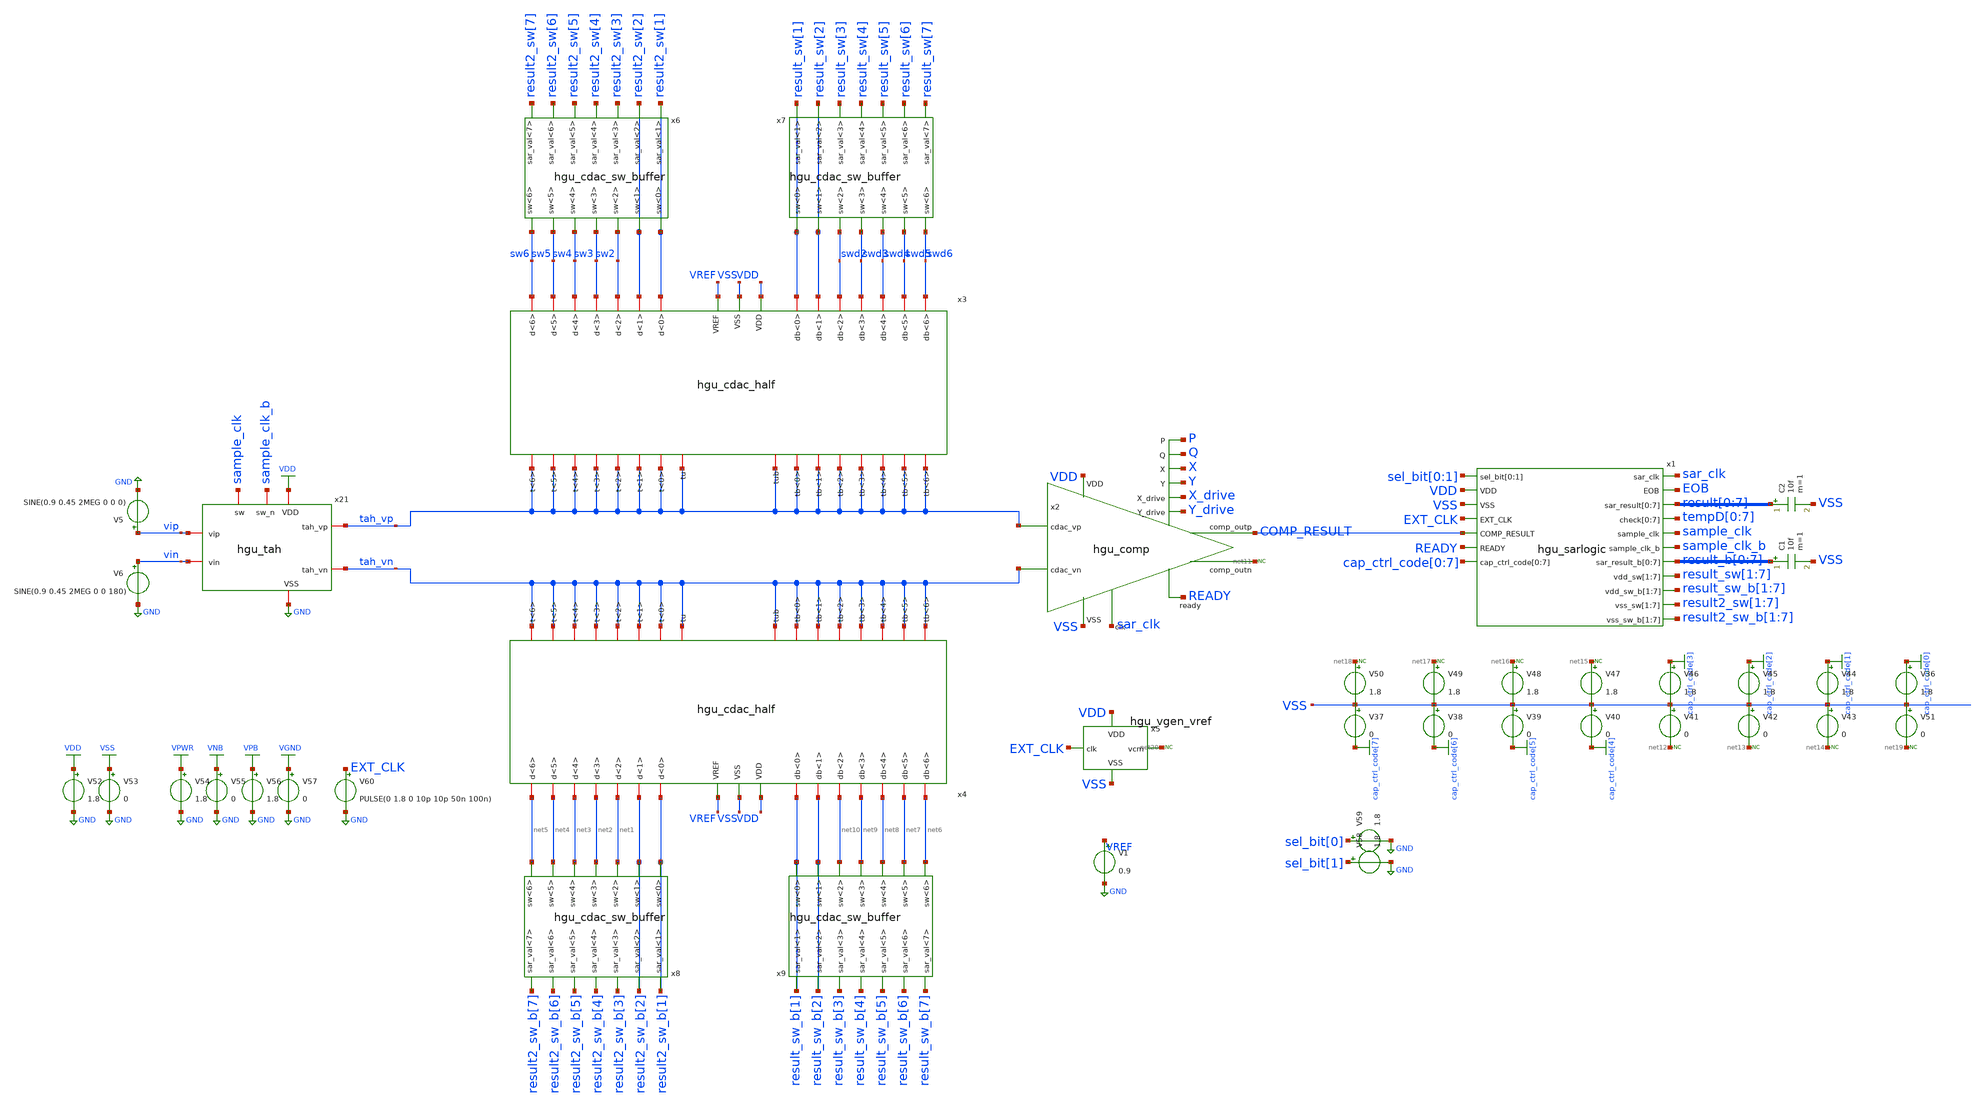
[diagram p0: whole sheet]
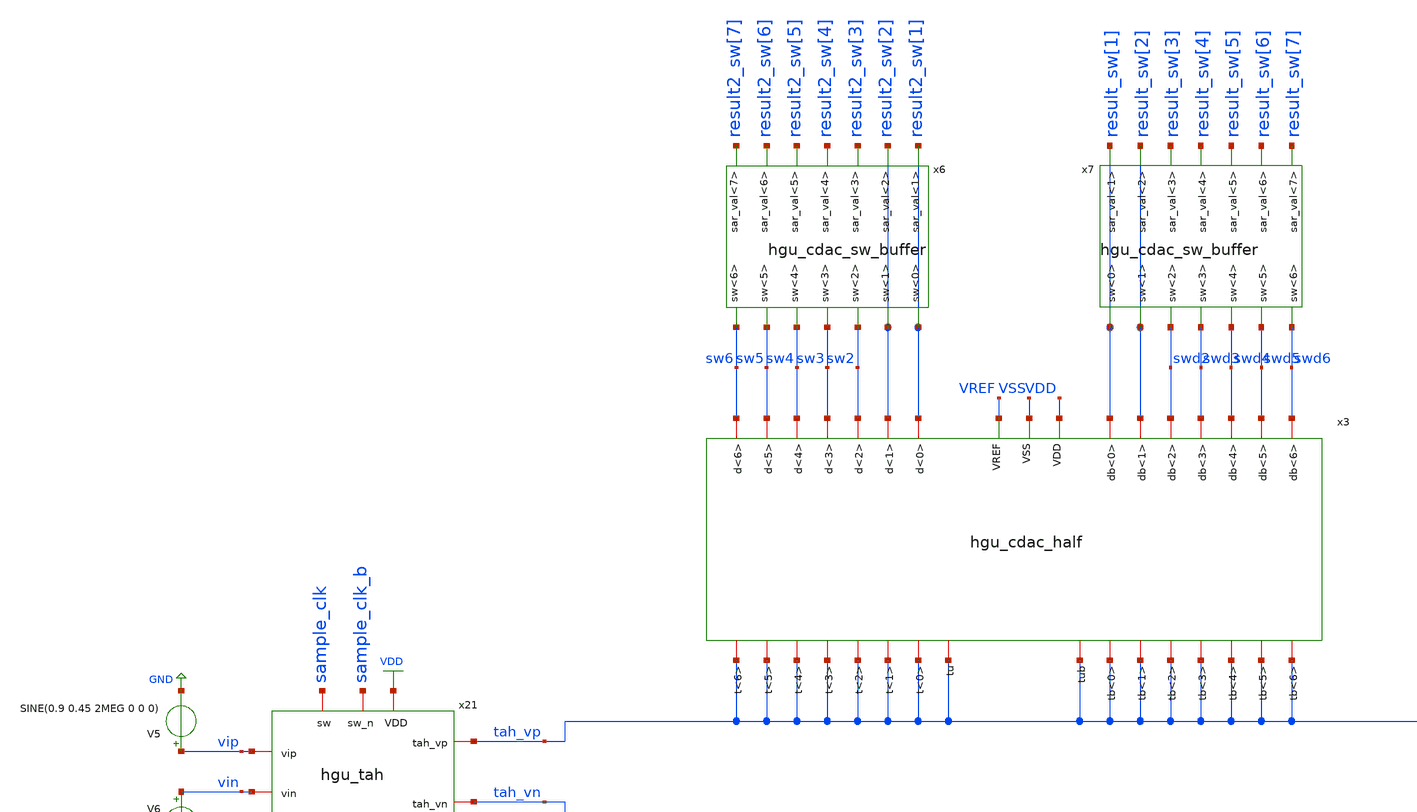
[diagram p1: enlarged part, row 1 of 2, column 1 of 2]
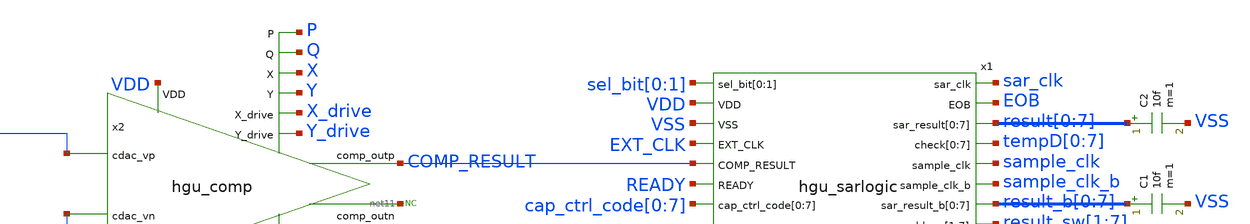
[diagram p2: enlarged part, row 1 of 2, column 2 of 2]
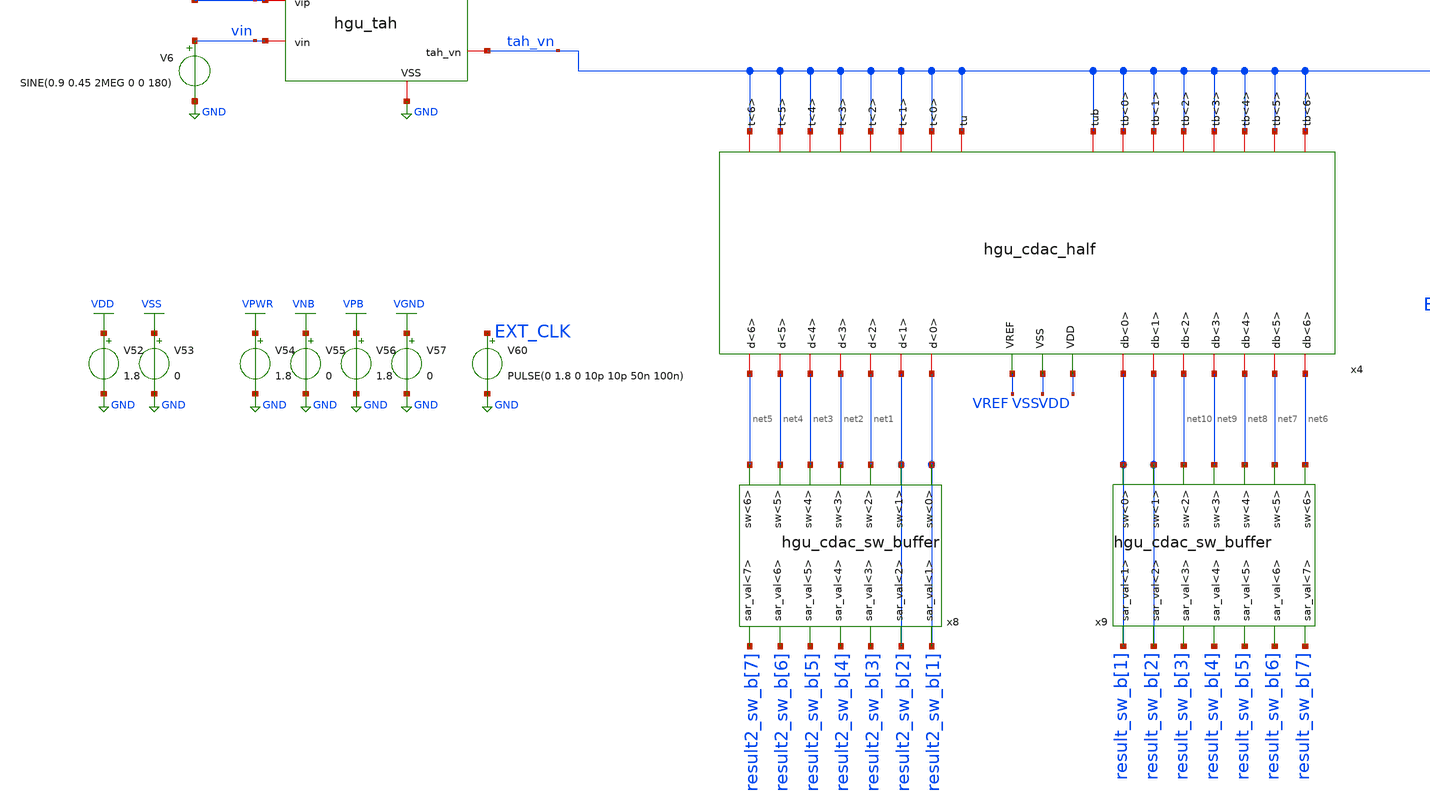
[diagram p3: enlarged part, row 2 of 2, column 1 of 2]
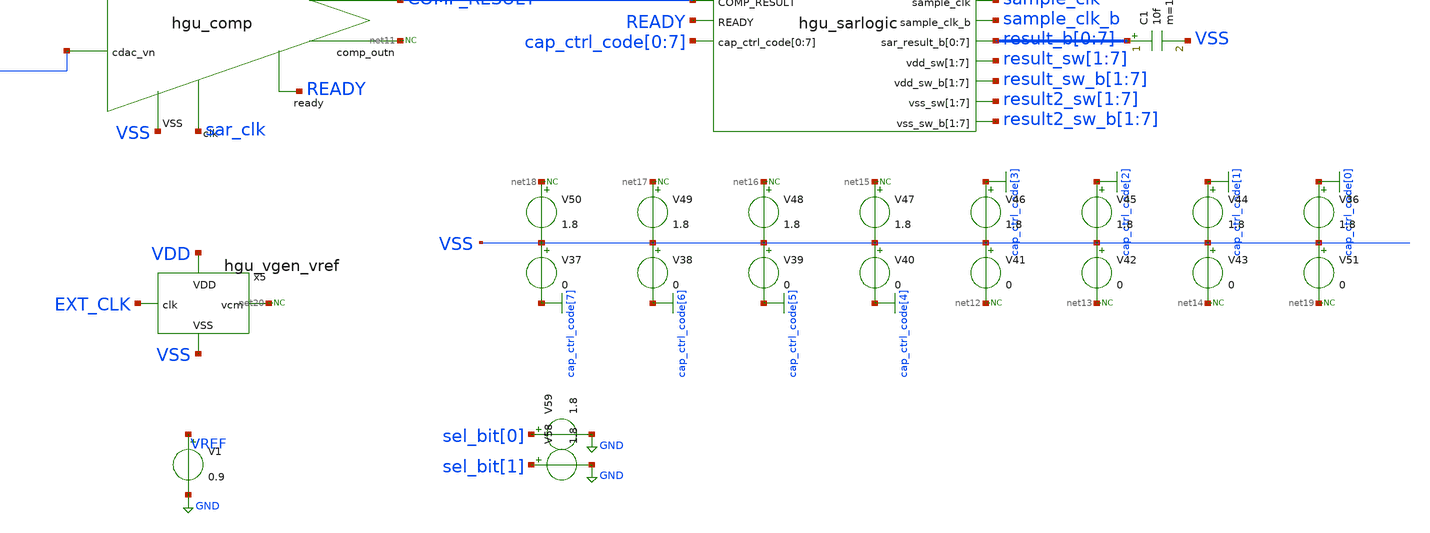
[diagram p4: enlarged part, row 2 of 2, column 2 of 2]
** sch_path: hgu/xschem/hgu_top.sch
**.subckt hgu_top
x1 sar_clk EOB result[0] result[1] result[2] result[3] result[4] result[5] result[6] result[7]
+ tempD[0] tempD[1] tempD[2] tempD[3] tempD[4] tempD[5] tempD[6] tempD[7] sample_clk sel_bit[0] sel_bit[1]
+ sample_clk_b VDD result_b[0] result_b[1] result_b[2] result_b[3] result_b[4] result_b[5] result_b[6] result_b[7]
+ VSS EXT_CLK COMP_RESULT READY result_sw[1] result_sw[2] result_sw[3] result_sw[4] result_sw[5]
+ result_sw[6] result_sw[7] result_sw_b[1] result_sw_b[2] result_sw_b[3] result_sw_b[4] result_sw_b[5]
+ result_sw_b[6] result_sw_b[7] result2_sw[1] result2_sw[2] result2_sw[3] result2_sw[4] result2_sw[5] result2_sw[6]
+ result2_sw[7] result2_sw_b[1] result2_sw_b[2] result2_sw_b[3] result2_sw_b[4] result2_sw_b[5] result2_sw_b[6]
+ result2_sw_b[7] cap_ctrl_code[0] cap_ctrl_code[1] cap_ctrl_code[2] cap_ctrl_code[3] cap_ctrl_code[4]
+ cap_ctrl_code[5] cap_ctrl_code[6] cap_ctrl_code[7] hgu_sarlogic
x2 Y X X_drive P Q READY tah_vn COMP_RESULT net11 tah_vp sar_clk Y_drive VDD VSS hgu_comp
x3 sw5 swd4 sw3 result_sw[2] swd2 sw2 swd6 swd5 result_sw[1] sw4 sw6 result2_sw[2] result2_sw[1]
+ swd3 VSS VREF tah_vp tah_vp tah_vp tah_vp tah_vp tah_vp tah_vp tah_vp tah_vp tah_vp tah_vp tah_vp tah_vp
+ tah_vp tah_vp tah_vp VDD hgu_cdac_half
x4 net4 net8 net2 result_sw_b[2] net10 net1 net6 net7 result_sw_b[1] net3 net5 result2_sw_b[2]
+ result2_sw_b[1] net9 VSS VREF tah_vn tah_vn tah_vn tah_vn tah_vn tah_vn tah_vn tah_vn tah_vn tah_vn tah_vn tah_vn
+ tah_vn tah_vn tah_vn tah_vn VDD hgu_cdac_half
x21 sample_clk VDD GND sample_clk_b tah_vp vip vin tah_vn hgu_tah
V5 vip GND SINE(0.9 0.45 2MEG 0 0 0)
V6 vin GND SINE(0.9 0.45 2MEG 0 0 180)
* noconn #net11
C2 result[0] VSS 10f m=1
V36 cap_ctrl_code[0] VSS 1.8
V37 VSS cap_ctrl_code[7] 0
V38 VSS cap_ctrl_code[6] 0
V39 VSS cap_ctrl_code[5] 0
V40 VSS cap_ctrl_code[4] 0
V41 VSS net12 0
V42 VSS net13 0
V43 VSS net14 0
V44 cap_ctrl_code[1] VSS 1.8
V45 cap_ctrl_code[2] VSS 1.8
V46 cap_ctrl_code[3] VSS 1.8
V47 net15 VSS 1.8
V48 net16 VSS 1.8
V49 net17 VSS 1.8
V50 net18 VSS 1.8
V51 VSS net19 0
* noconn #net18
* noconn #net17
* noconn #net16
* noconn #net15
* noconn #net12
* noconn #net13
* noconn #net14
* noconn #net19
V52 VDD GND 1.8
V53 VSS GND 0
V54 VPWR GND 1.8
V55 VNB GND 0
V56 VPB GND 1.8
V57 VGND GND 0
V60 EXT_CLK GND PULSE(0 1.8 0 10p 10p 50n 100n)
x5 VDD VSS EXT_CLK net20 hgu_vgen_vref
C1 result_b[0] VSS 10f m=1
V58 sel_bit[1] GND 1.8
V59 sel_bit[0] GND 1.8
x6 result2_sw[3] result2_sw[6] result2_sw[1] result2_sw[2] result2_sw[4] result2_sw[5] result2_sw[7]
+ result2_sw[2] sw2 sw5 sw3 result2_sw[1] sw4 sw6 hgu_cdac_sw_buffer
x7 result_sw[3] result_sw[6] result_sw[1] result_sw[2] result_sw[4] result_sw[5] result_sw[7]
+ result_sw[2] swd2 swd5 swd3 result_sw[1] swd4 swd6 hgu_cdac_sw_buffer
x8 result2_sw_b[3] result2_sw_b[6] result2_sw_b[1] result2_sw_b[2] result2_sw_b[4] result2_sw_b[5]
+ result2_sw_b[7] result2_sw_b[2] net1 net4 net2 result2_sw_b[1] net3 net5 hgu_cdac_sw_buffer
x9 result_sw_b[3] result_sw_b[6] result_sw_b[1] result_sw_b[2] result_sw_b[4] result_sw_b[5]
+ result_sw_b[7] result_sw_b[2] net10 net7 net9 result_sw_b[1] net8 net6 hgu_cdac_sw_buffer
V1 VREF GND 0.9
* noconn #net20
**** begin user architecture code



.lib /foss/pdks/sky130A/libs.tech/ngspice/sky130.lib.spice tt
.include /foss/pdks/sky130A/libs.ref/sky130_fd_sc_hd/spice/sky130_fd_sc_hd.spice
.include /foss/designs/hgu_goss/hgu/mag/hgu_cdac_unit.spice

.OPTIONS savecurrents
.tran 10ps 800ns

.control
	run
	plot V(sample_clk) V(vip) V(vin) V(vip)-V(vin)+0.9 V(tah_vp) V(tah_vn) V(tah_vp)-V(tah_vn)
+ V(vip)-V(vin)
	plot V(EXT_CLK)-2 V(sample_clk) V(sample_clk_b) V(EOB)+2 V(READY)+4 V(sar_clk)+6 V(COMP_RESULT)+8
	plot V("tempD[0]") V("tempD[1]")+2 V("tempD[2]")+4 V("tempD[3]")+6 V("tempD[4]")+8 V("tempD[5]")+10
+ V("tempD[6]")+12 V("tempD[7]")+14 V(sar_clk) V(sar_clk)+2 V(sar_clk)+4 V(sar_clk)+6 V(sar_clk)+8 V(sar_clk)+10
+ V(sar_clk)+12 V(sar_clk)+14 V(EOB)-2
	*plot V("result_sw[1]")+2 V("result_sw[2]")+4 V("result_sw[3]")+6 V("result_sw[4]")+8
+ V("result_sw[5]")+10 V("result_sw[6]")+12 V("result_sw[7]")+14 V("result2_sw[1]")+2 V("result2_sw[2]")+4
+ V("result2_sw[3]")+6 V("result2_sw[4]")+8 V("result2_sw[5]")+10 V("result2_sw[6]")+12 V("result2_sw[7]")+14
 	*plot V(vip)-V(vin)+0.9 V(X)+2 V(Y)+2 V(Q)-2 V(P)-2 V(X_drive)+4 V(Y_drive)+4
	plot V("result_sw[1]")+2 V("result_sw[2]")+4 V("result_sw[3]")+6 V("result_sw[4]")+8
+ V("result_sw[5]")+10 V("result_sw[6]")+12 V("result_sw[7]")+14 V("result2_sw[1]")+2 V("result2_sw[2]")+4
+ V("result2_sw[3]")+6 V("result2_sw[4]")+8 V("result2_sw[5]")+10 V("result2_sw[6]")+12 V("result2_sw[7]")+14
+ V("result_sw_b[1]")+2 V("result_sw_b[2]")+4 V("result_sw_b[3]")+6 V("result_sw_b[4]")+8 V("result_sw_b[5]")+10
+ V("result_sw_b[6]")+12 V("result_sw_b[7]")+14 V("result2_sw_b[1]")+2 V("result2_sw_b[2]")+4 V("result2_sw_b[3]")+6
+ V("result2_sw_b[4]")+8 V("result2_sw_b[5]")+10 V("result2_sw_b[6]")+12 V("result2_sw_b[7]")+14



.endc
.save all



**** end user architecture code
**.ends
.GLOBAL GND
.GLOBAL VDD
.GLOBAL cap_ctrl_code[7]
.GLOBAL cap_ctrl_code[6]
.GLOBAL cap_ctrl_code[5]
.GLOBAL cap_ctrl_code[4]
.GLOBAL cap_ctrl_code[3]
.GLOBAL cap_ctrl_code[2]
.GLOBAL cap_ctrl_code[1]
.GLOBAL cap_ctrl_code[0]
.GLOBAL VSS
.GLOBAL VGND
.GLOBAL VNB
.GLOBAL VPB
.GLOBAL VPWR
.end
